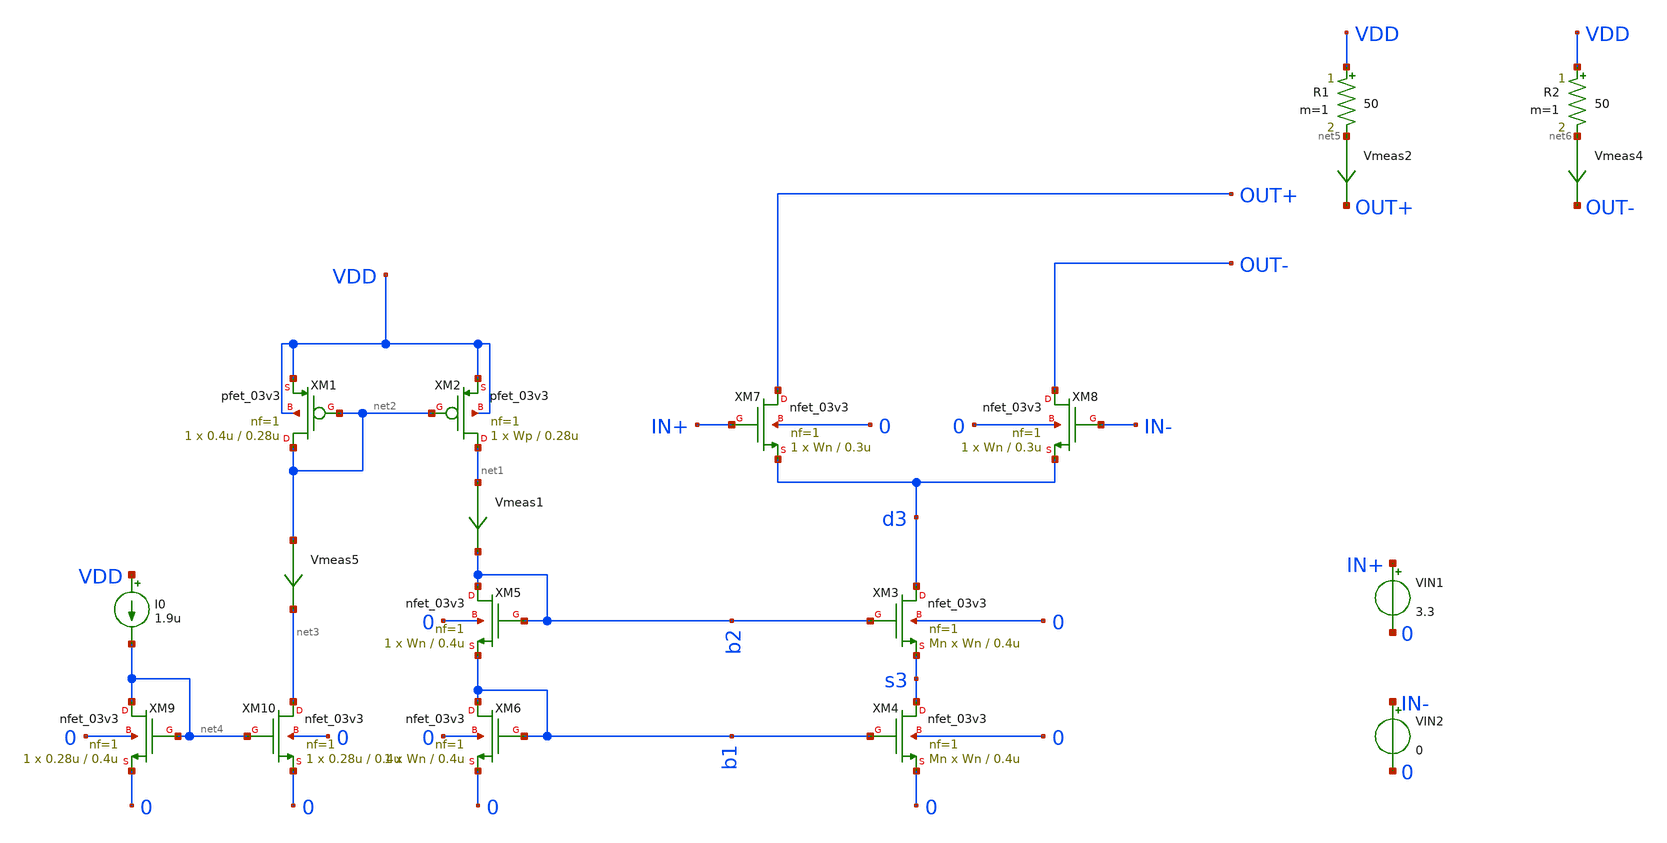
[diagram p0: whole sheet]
** sch_path: DAC/xschem/analog_cell/test/test)cascode_current_unit.sch
**.subckt test)cascode_current_unit
XM3 d3 b2 s3 0 nfet_03v3 L=0.4u W=Wn nf=1 ad='int((nf+1)/2) * W/nf * 0.18u' as='int((nf+2)/2) * W/nf * 0.18u'
+ pd='2*int((nf+1)/2) * (W/nf + 0.18u)' ps='2*int((nf+2)/2) * (W/nf + 0.18u)' nrd='0.18u / W' nrs='0.18u / W'
+ sa=0 sb=0 sd=0 m=Mn
XM4 s3 b1 0 0 nfet_03v3 L=0.4u W=Wn nf=1 ad='int((nf+1)/2) * W/nf * 0.18u' as='int((nf+2)/2) * W/nf * 0.18u'
+ pd='2*int((nf+1)/2) * (W/nf + 0.18u)' ps='2*int((nf+2)/2) * (W/nf + 0.18u)' nrd='0.18u / W' nrs='0.18u / W'
+ sa=0 sb=0 sd=0 m=Mn
XM5 b2 b2 b1 0 nfet_03v3 L=0.4u W=Wn nf=1 ad='int((nf+1)/2) * W/nf * 0.18u' as='int((nf+2)/2) * W/nf * 0.18u'
+ pd='2*int((nf+1)/2) * (W/nf + 0.18u)' ps='2*int((nf+2)/2) * (W/nf + 0.18u)' nrd='0.18u / W' nrs='0.18u / W'
+ sa=0 sb=0 sd=0 m=1
XM6 b1 b1 0 0 nfet_03v3 L=0.4u W=Wn nf=1 ad='int((nf+1)/2) * W/nf * 0.18u' as='int((nf+2)/2) * W/nf * 0.18u'
+ pd='2*int((nf+1)/2) * (W/nf + 0.18u)' ps='2*int((nf+2)/2) * (W/nf + 0.18u)' nrd='0.18u / W' nrs='0.18u / W'
+ sa=0 sb=0 sd=0 m=1
Vmeas1 net1 b2 0
.save i(vmeas1)
XM1 net2 net2 VDD VDD pfet_03v3 L=0.28u W=0.4u nf=1 ad='int((nf+1)/2) * W/nf * 0.18u' as='int((nf+2)/2) * W/nf * 0.18u'
+ pd='2*int((nf+1)/2) * (W/nf + 0.18u)' ps='2*int((nf+2)/2) * (W/nf + 0.18u)' nrd='0.18u / W' nrs='0.18u / W'
+ sa=0 sb=0 sd=0 m=1
XM2 net1 net2 VDD VDD pfet_03v3 L=0.28u W=Wp nf=1 ad='int((nf+1)/2) * W/nf * 0.18u' as='int((nf+2)/2) * W/nf * 0.18u'
+ pd='2*int((nf+1)/2) * (W/nf + 0.18u)' ps='2*int((nf+2)/2) * (W/nf + 0.18u)' nrd='0.18u / W' nrs='0.18u / W'
+ sa=0 sb=0 sd=0 m=1
XM7 OUT+ IN+ d3 0 nfet_03v3 L=0.3u W=Wn nf=1 ad='int((nf+1)/2) * W/nf * 0.18u' as='int((nf+2)/2) * W/nf * 0.18u'
+ pd='2*int((nf+1)/2) * (W/nf + 0.18u)' ps='2*int((nf+2)/2) * (W/nf + 0.18u)' nrd='0.18u / W' nrs='0.18u / W'
+ sa=0 sb=0 sd=0 m=1
XM8 OUT- IN- d3 0 nfet_03v3 L=0.3u W=Wn nf=1 ad='int((nf+1)/2) * W/nf * 0.18u' as='int((nf+2)/2) * W/nf * 0.18u'
+ pd='2*int((nf+1)/2) * (W/nf + 0.18u)' ps='2*int((nf+2)/2) * (W/nf + 0.18u)' nrd='0.18u / W' nrs='0.18u / W'
+ sa=0 sb=0 sd=0 m=1
R1 VDD net5 50 m=1
R2 VDD net6 50 m=1
Vmeas2 net5 OUT+ 0
.save i(vmeas2)
Vmeas4 net6 OUT- 0
.save i(vmeas4)
VIN1 IN+ 0 3.3
VIN2 IN- 0 0
I0 VDD net4 1.9u
Vmeas5 net2 net3 0
.save i(vmeas5)
XM9 net4 net4 0 0 nfet_03v3 L=0.4u W=0.28u nf=1 ad='int((nf+1)/2) * W/nf * 0.18u' as='int((nf+2)/2) * W/nf * 0.18u'
+ pd='2*int((nf+1)/2) * (W/nf + 0.18u)' ps='2*int((nf+2)/2) * (W/nf + 0.18u)' nrd='0.18u / W' nrs='0.18u / W'
+ sa=0 sb=0 sd=0 m=1
XM10 net3 net4 0 0 nfet_03v3 L=0.4u W=0.28u nf=1 ad='int((nf+1)/2) * W/nf * 0.18u' as='int((nf+2)/2) * W/nf * 0.18u'
+ pd='2*int((nf+1)/2) * (W/nf + 0.18u)' ps='2*int((nf+2)/2) * (W/nf + 0.18u)' nrd='0.18u / W' nrs='0.18u / W'
+ sa=0 sb=0 sd=0 m=1
**** begin user architecture code

.include $::180MCU_MODELS/design.ngspice
.lib $::180MCU_MODELS/sm141064.ngspice typical
.lib $::180MCU_MODELS/sm141064.ngspice res_typical
.lib $::180MCU_MODELS/sm141064.ngspice moscap_typical
* .lib $::180MCU_MODELS/sm141064.ngspice res_statistical



V0 VDD 0 3.3
*V1 IN+ 0 3
*V2 IN- 0 0

.options savecurrents
.param Wn=0.3u
.param Wp=1.8u
.param Mn=1

.control
	dc I0 1u 4u 0.1u
	*tran 1u 100u

	plot v(d3)
 	plot v(b2)-v(s3)-@m.xm3.m0[vth] v(b1)-@m.xm4.m0[vth]
	plot @m.xm3.m0[vth] @m.xm4.m0[vth]
	plot V(IN+) V(IN-)
	plot i(Vmeas1) i(Vmeas2)

.endc

.save all @m.xm1.m0[vth] @m.xm2.m0[vth] @m.xm3.m0[vth] @m.xm4.m0[vth]


**** end user architecture code
**.ends
.end
